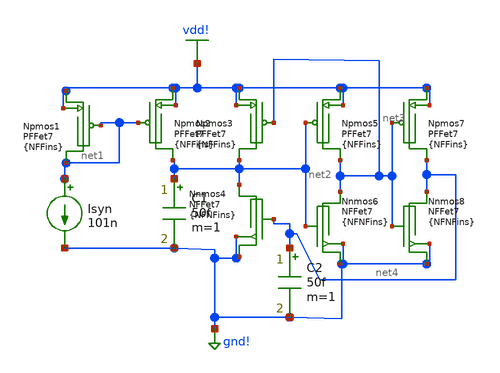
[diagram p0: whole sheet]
** sch_path: SimulationModeling/Besrour.sch
**.subckt Besrour
Npmos2 vdd! net1 net2 vdd! BSIMCMG_osdi_P nfin={NFFins}
Npmos5 vdd! net2 net3 vdd! BSIMCMG_osdi_P nfin={NFFins}
Npmos7 vdd! net3 net4 vdd! BSIMCMG_osdi_P nfin={NFFins}
Nnmos6 gnd! net2 net3 gnd! BSIMCMG_osdi_N nfin={NFNFins}
Nnmos8 gnd! net3 net4 gnd! BSIMCMG_osdi_N nfin={NFNFins}
C2 net4 gnd! 50f m=1
C1 net2 gnd! 50f m=1
Npmos1 vdd! net1 net1 vdd! BSIMCMG_osdi_P nfin={NFFins}
Npmos3 vdd! net3 net2 vdd! BSIMCMG_osdi_P nfin={NFFins}
Nnmos4 gnd! net4 net2 gnd! BSIMCMG_osdi_N nfin={NFNFins}
Isyn net1 gnd! 101n
**** begin user architecture code



* ngspice commands
.include asap7_TT_slvt.sp
.param NFFins=1
.param NFNFins=5
Vvdd vdd! 0 dc=0.7
Vgnd gnd! 0 dc=0
.ic v(net2)=0 v(net4)=0
.control
    set maxstep = 0.01n

    set method = gear
    set gmin = 1e-15

    set itl1 = 1000
    set itl4 = 1000
    set num_threads = 24
    set parallel = 1
    set filetype=ascii
    set wr_vecnames
    set wr_singlescale

    echo VDD Cap1 Cap2 Spikes Frequency Energy_Per_Spike > /Users/logan/Desktop/besourneuron.txt

    alter Isyn = 100n

    foreach vdd 0.1 0.11 0.12 0.13 0.14 0.15 0.16 0.17 0.18 0.19 0.2 0.21 0.22 0.23 0.24 0.25 0.26
+ 0.27 0.28 0.29 0.3 0.31 0.32 0.33 0.34 0.35 0.36 0.37 0.38 0.39 0.4 0.41 0.42 0.43 0.44 0.45 0.46 0.47
+ 0.48 0.49 0.5 0.51 0.52 0.53 0.54 0.55 0.56 0.57 0.58 0.59 0.6 0.61 0.62 0.63 0.64 0.65 0.66 0.67 0.68
+ 0.69 0.7 0.71 0.72 0.73 0.74 0.75 0.76 0.77 0.78 0.79 0.8 0.81 0.82 0.83 0.84 0.85 0.86 0.87 0.88 0.89
+ 0.9
        alter Vvdd dc=$vdd
        let vth = 0.2 * $vdd
        let low_th = 0.05 * $vdd

        foreach cap1 0.1e-15 0.2e-15 0.3e-15 0.4e-15 0.5e-15 0.6e-15 0.7e-15 0.8e-15 0.9e-15 1e-15
+ 2e-15 3e-15 4e-15 5e-15 6e-15 7e-15 8e-15 9e-15 10e-15
            alter C1 = $cap1

            foreach cap2 0.1e-15 0.2e-15 0.3e-15 0.4e-15 0.5e-15 0.6e-15 0.7e-15 0.8e-15 0.9e-15
+ 1e-15 2e-15 3e-15 4e-15 5e-15 6e-15 7e-15 8e-15 9e-15 10e-15
                alter C2 = $cap2

                tran 0.04n 20n UIC

                let power_vdd = -1*v(vdd!)*i(Vvdd)
                let dt = time[1] - time[0]

                let transitions = vector(length(v(net4)))
                let i = 0
                let count = 0
                let last_state = 0
                let spike_energy = 0
                let current_spike_energy = 0

                dowhile i < length(v(net4))-1
                    if (v(net4)[i] gt $&vth and last_state eq 0)
                        let count = count + 1
                        let last_state = 1
                        let current_spike_energy = 0
                    end
                    if (last_state eq 1)
                        let current_spike_energy = current_spike_energy + power_vdd[i] * $&dt
                    end
                    if (v(net4)[i] lt $&low_th)
                        if (last_state eq 1)
                            let spike_energy = spike_energy + current_spike_energy
                        end
                        let last_state = 0
                    end
                    let i = i + 1
                end

                let spike_count = $&count
                let sim_time = 20e-9
                let spiking_freq = $&spike_count / sim_time
                let energy_per_spike = 0
                if spike_count gt 0
                    let energy_per_spike = (spike_energy / spike_count)
                end

                echo $vdd $cap1 $cap2 $&spike_count $&spiking_freq $&energy_per_spike >>
+ /Users/logan/Desktop/besourneuron.txt
                echo At VDD=$vdd V Cap1=$cap1 F Cap2=$cap2 F Spikes=$&spike_count Spikes
+ Freq=$&spiking_freq Hz Energy/Spike=$&energy_per_spike J
            end
        end
    end
.endc



**** end user architecture code
**.ends
.GLOBAL vdd!
.GLOBAL gnd!
.end
